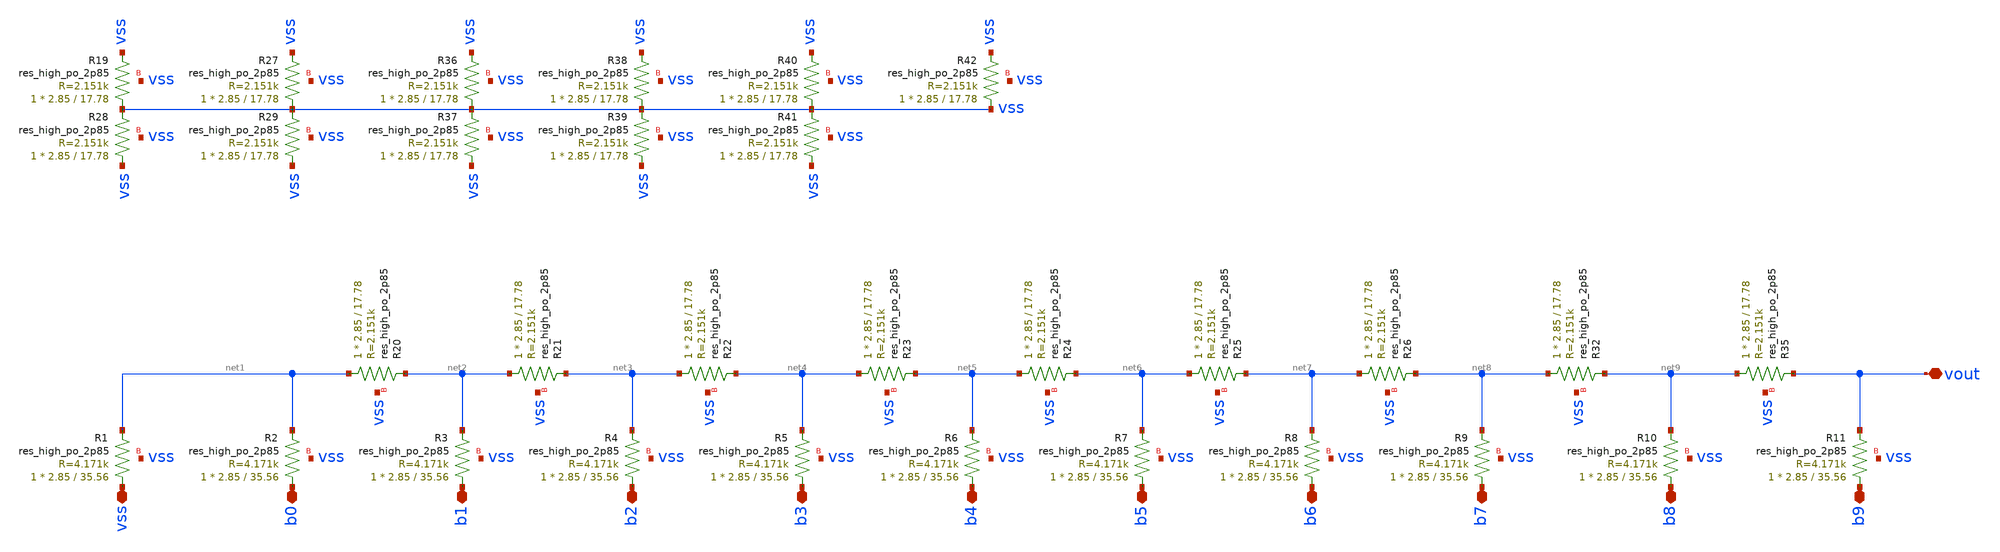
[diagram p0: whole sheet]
** sch_path: xschem/r2r_10.sch
**.subckt r2r_10 b0 vss vout b1 b2 b3 b4 b5 b6 b7 b8 b9
*.iopin b0
*.iopin vss
*.iopin vout
*.iopin b1
*.iopin b2
*.iopin b3
*.iopin b4
*.iopin b5
*.iopin b6
*.iopin b7
*.iopin b8
*.iopin b9
XR20 net1 net2 vss sky130_fd_pr__res_high_po_2p85 L=17.78 mult=1 m=1
XR21 net2 net3 vss sky130_fd_pr__res_high_po_2p85 L=17.78 mult=1 m=1
XR22 net3 net4 vss sky130_fd_pr__res_high_po_2p85 L=17.78 mult=1 m=1
XR23 net4 net5 vss sky130_fd_pr__res_high_po_2p85 L=17.78 mult=1 m=1
XR24 net5 net6 vss sky130_fd_pr__res_high_po_2p85 L=17.78 mult=1 m=1
XR25 net6 net7 vss sky130_fd_pr__res_high_po_2p85 L=17.78 mult=1 m=1
XR26 net7 net8 vss sky130_fd_pr__res_high_po_2p85 L=17.78 mult=1 m=1
XR19 vss vss vss sky130_fd_pr__res_high_po_2p85 L=17.78 mult=1 m=1
XR27 vss vss vss sky130_fd_pr__res_high_po_2p85 L=17.78 mult=1 m=1
XR28 vss vss vss sky130_fd_pr__res_high_po_2p85 L=17.78 mult=1 m=1
XR29 vss vss vss sky130_fd_pr__res_high_po_2p85 L=17.78 mult=1 m=1
XR32 net8 net9 vss sky130_fd_pr__res_high_po_2p85 L=17.78 mult=1 m=1
XR35 net9 vout vss sky130_fd_pr__res_high_po_2p85 L=17.78 mult=1 m=1
XR36 vss vss vss sky130_fd_pr__res_high_po_2p85 L=17.78 mult=1 m=1
XR37 vss vss vss sky130_fd_pr__res_high_po_2p85 L=17.78 mult=1 m=1
XR38 vss vss vss sky130_fd_pr__res_high_po_2p85 L=17.78 mult=1 m=1
XR39 vss vss vss sky130_fd_pr__res_high_po_2p85 L=17.78 mult=1 m=1
XR40 vss vss vss sky130_fd_pr__res_high_po_2p85 L=17.78 mult=1 m=1
XR41 vss vss vss sky130_fd_pr__res_high_po_2p85 L=17.78 mult=1 m=1
XR42 vss vss vss sky130_fd_pr__res_high_po_2p85 L=17.78 mult=1 m=1
XR1 vss net1 vss sky130_fd_pr__res_high_po_2p85 L=35.56 mult=1 m=1
XR2 b0 net1 vss sky130_fd_pr__res_high_po_2p85 L=35.56 mult=1 m=1
XR3 b1 net2 vss sky130_fd_pr__res_high_po_2p85 L=35.56 mult=1 m=1
XR4 b2 net3 vss sky130_fd_pr__res_high_po_2p85 L=35.56 mult=1 m=1
XR5 b3 net4 vss sky130_fd_pr__res_high_po_2p85 L=35.56 mult=1 m=1
XR6 b4 net5 vss sky130_fd_pr__res_high_po_2p85 L=35.56 mult=1 m=1
XR7 b5 net6 vss sky130_fd_pr__res_high_po_2p85 L=35.56 mult=1 m=1
XR8 b6 net7 vss sky130_fd_pr__res_high_po_2p85 L=35.56 mult=1 m=1
XR9 b7 net8 vss sky130_fd_pr__res_high_po_2p85 L=35.56 mult=1 m=1
XR10 b8 net9 vss sky130_fd_pr__res_high_po_2p85 L=35.56 mult=1 m=1
XR11 b9 vout vss sky130_fd_pr__res_high_po_2p85 L=35.56 mult=1 m=1
**.ends
.end
